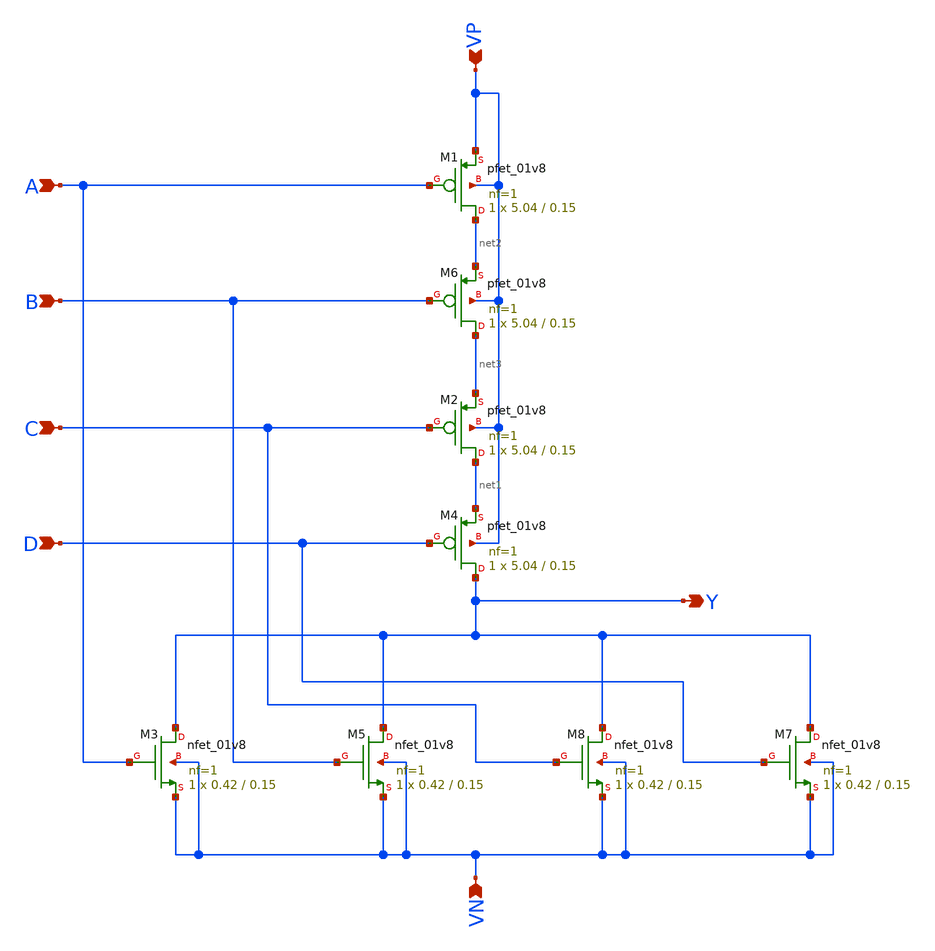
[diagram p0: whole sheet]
** sch_path: component/NOR4/nor4.sch
**.subckt nor4 Y C D A B VP VN
*.opin Y
*.ipin C
*.ipin D
*.ipin A
*.ipin B
*.ipin VP
*.ipin VN
XM5 Y B VN VN sky130_fd_pr__nfet_01v8 L=0.15 W=0.42 nf=1 ad='int((nf+1)/2) * W/nf * 0.29' as='int((nf+2)/2) * W/nf * 0.29'
+ pd='2*int((nf+1)/2) * (W/nf + 0.29)' ps='2*int((nf+2)/2) * (W/nf + 0.29)' nrd='0.29 / W' nrs='0.29 / W'
+ sa=0 sb=0 sd=0 mult=1 m=1
XM3 Y A VN VN sky130_fd_pr__nfet_01v8 L=0.15 W=0.42 nf=1 ad='int((nf+1)/2) * W/nf * 0.29' as='int((nf+2)/2) * W/nf * 0.29'
+ pd='2*int((nf+1)/2) * (W/nf + 0.29)' ps='2*int((nf+2)/2) * (W/nf + 0.29)' nrd='0.29 / W' nrs='0.29 / W'
+ sa=0 sb=0 sd=0 mult=1 m=1
XM2 net1 C net3 VP sky130_fd_pr__pfet_01v8 L=0.15 W=5.04 nf=1 ad='int((nf+1)/2) * W/nf * 0.29' as='int((nf+2)/2) * W/nf * 0.29'
+ pd='2*int((nf+1)/2) * (W/nf + 0.29)' ps='2*int((nf+2)/2) * (W/nf + 0.29)' nrd='0.29 / W' nrs='0.29 / W'
+ sa=0 sb=0 sd=0 mult=1 m=1
XM4 Y D net1 VP sky130_fd_pr__pfet_01v8 L=0.15 W=5.04 nf=1 ad='int((nf+1)/2) * W/nf * 0.29' as='int((nf+2)/2) * W/nf * 0.29'
+ pd='2*int((nf+1)/2) * (W/nf + 0.29)' ps='2*int((nf+2)/2) * (W/nf + 0.29)' nrd='0.29 / W' nrs='0.29 / W'
+ sa=0 sb=0 sd=0 mult=1 m=1
XM1 net2 A VP VP sky130_fd_pr__pfet_01v8 L=0.15 W=5.04 nf=1 ad='int((nf+1)/2) * W/nf * 0.29' as='int((nf+2)/2) * W/nf * 0.29'
+ pd='2*int((nf+1)/2) * (W/nf + 0.29)' ps='2*int((nf+2)/2) * (W/nf + 0.29)' nrd='0.29 / W' nrs='0.29 / W'
+ sa=0 sb=0 sd=0 mult=1 m=1
XM6 net3 B net2 VP sky130_fd_pr__pfet_01v8 L=0.15 W=5.04 nf=1 ad='int((nf+1)/2) * W/nf * 0.29' as='int((nf+2)/2) * W/nf * 0.29'
+ pd='2*int((nf+1)/2) * (W/nf + 0.29)' ps='2*int((nf+2)/2) * (W/nf + 0.29)' nrd='0.29 / W' nrs='0.29 / W'
+ sa=0 sb=0 sd=0 mult=1 m=1
XM7 Y D VN VN sky130_fd_pr__nfet_01v8 L=0.15 W=0.42 nf=1 ad='int((nf+1)/2) * W/nf * 0.29' as='int((nf+2)/2) * W/nf * 0.29'
+ pd='2*int((nf+1)/2) * (W/nf + 0.29)' ps='2*int((nf+2)/2) * (W/nf + 0.29)' nrd='0.29 / W' nrs='0.29 / W'
+ sa=0 sb=0 sd=0 mult=1 m=1
XM8 Y C VN VN sky130_fd_pr__nfet_01v8 L=0.15 W=0.42 nf=1 ad='int((nf+1)/2) * W/nf * 0.29' as='int((nf+2)/2) * W/nf * 0.29'
+ pd='2*int((nf+1)/2) * (W/nf + 0.29)' ps='2*int((nf+2)/2) * (W/nf + 0.29)' nrd='0.29 / W' nrs='0.29 / W'
+ sa=0 sb=0 sd=0 mult=1 m=1
**.ends
.end
